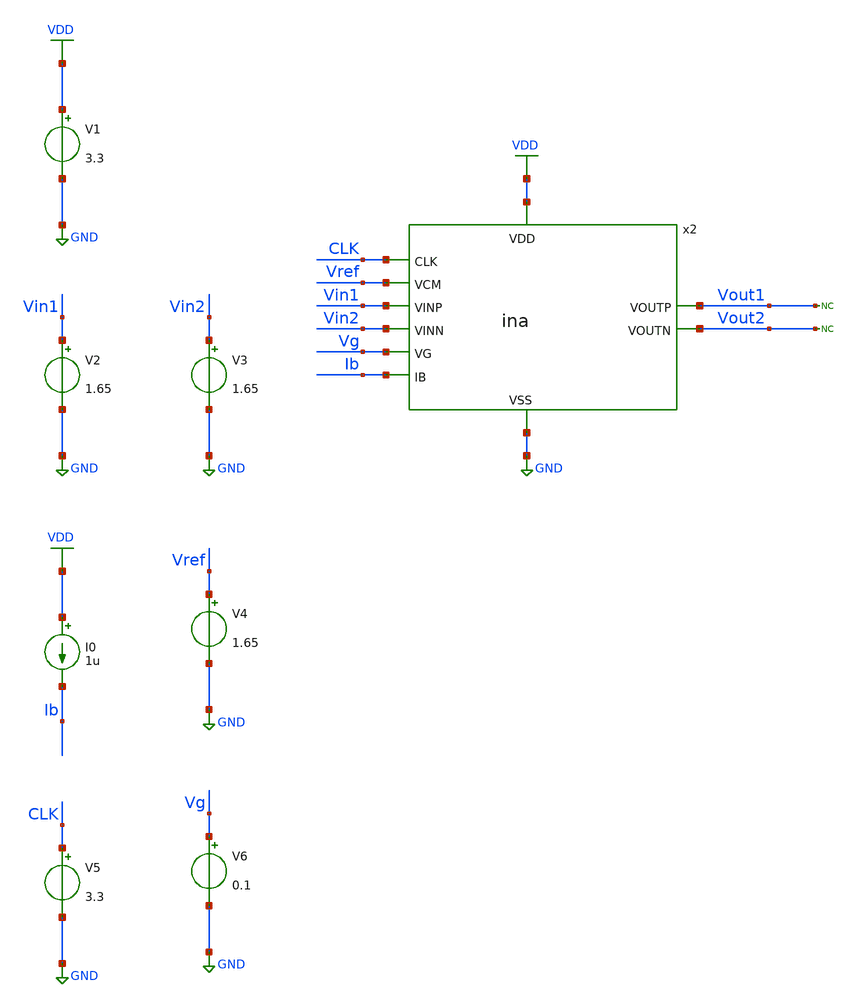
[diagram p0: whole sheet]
** sch_path: designs/libs/tb_ina/tb_ina_psrr/tb_ina_psrr.sch
**.subckt tb_ina_psrr
V1 VDD GND 3.3
V2 Vin1 GND 1.65
V3 Vin2 GND 1.65
I0 VDD Ib 1u
V4 Vref GND 1.65
x2 Vg VDD Vin1 Vin2 CLK Vout1 Vout2 GND Vref Ib ina
V5 CLK GND 3.3
V6 Vg GND 0.1
* noconn Vout1
* noconn Vout2
**** begin user architecture code

.include $::180MCU_MODELS/design.ngspice
.lib $::180MCU_MODELS/sm141064.ngspice typical
.lib $::180MCU_MODELS/sm141064.ngspice cap_mim
.lib $::180MCU_MODELS/sm141064.ngspice moscap_typical
.lib $::180MCU_MODELS/sm141064.ngspice mimcap_typical
.lib $::180MCU_MODELS/sm141064.ngspice res_typical
* .lib $::180MCU_MODELS/sm141064.ngspice res_statistical
* ngspice commands




.control
save all

run
set color0 = white

*************************************
** PARAMETERS
*************************************

let Vdd  = 3.3
let Vcm  = 1.65
let Ibias = 2u
let Vg  = 0.1

*************************************
** CHOPPER PARAMETERS
*************************************

let fchop = 4k
let tper = 1/fchop
let ton = tper/2
let tr = 10n
let tf = 10n

*************************************
** SOURCES
*************************************

alter @V1[DC] = $&Vdd
alter @V1[ACMAG] = 1
alter @V2[DC] = $&Vcm
alter @V3[DC] = $&Vcm
alter @V4[DC] = $&Vcm
alter @I0[DC] = $&Ibias
alter @V5[PULSE] = [ 0 $&Vdd 0 $&tr $&tf $&ton $&tper 0 ]
alter @V6[DC] = $&Vg

*************************************
** AC SIMULATION
*************************************

ac dec 100 0.01 1G

*************************************
** MEASUREMENTS
*************************************

let Aps = v(Vout1)/1
let psrr_db = -db(Aps)
meas ac psrr_gain FIND psrr_db AT=10
let psrr_3db = psrr_gain - 3
meas ac psrr_bw WHEN psrr_db=$&psrr_3db
print psrr_gain
print psrr_bw

*************************************
** PLOTS
*************************************

plot psrr_db

*************************************
** SAVE
*************************************

write tb_ina_psrr.raw

.endc
* ngspice commands



**** end user architecture code
**.ends
.GLOBAL GND
.GLOBAL VDD
.end
